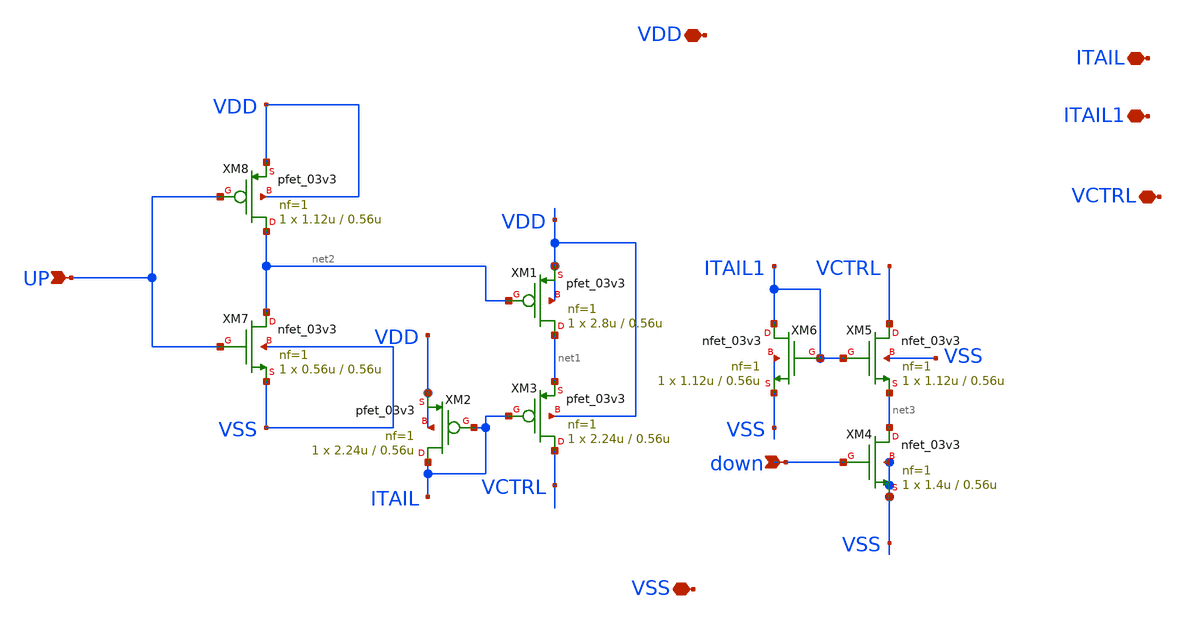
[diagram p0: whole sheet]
** sch_path: PLL-main/schematic/xschem/CP.sch
**.subckt CP UP down VCTRL VDD VSS ITAIL1 ITAIL
*.ipin UP
*.ipin down
*.iopin VCTRL
*.iopin VDD
*.iopin VSS
*.iopin ITAIL1
*.iopin ITAIL
XM1 net1 net2 VDD VDD pfet_03v3 L=0.56u W=2.8u nf=1 ad='int((nf+1)/2) * W/nf * 0.18u' as='int((nf+2)/2) * W/nf * 0.18u'
+ pd='2*int((nf+1)/2) * (W/nf + 0.18u)' ps='2*int((nf+2)/2) * (W/nf + 0.18u)' nrd='0.18u / W' nrs='0.18u / W'
+ sa=0 sb=0 sd=0 m=1
XM3 VCTRL ITAIL net1 VDD pfet_03v3 L=0.56u W=2.24u nf=1 ad='int((nf+1)/2) * W/nf * 0.18u' as='int((nf+2)/2) * W/nf * 0.18u'
+ pd='2*int((nf+1)/2) * (W/nf + 0.18u)' ps='2*int((nf+2)/2) * (W/nf + 0.18u)' nrd='0.18u / W' nrs='0.18u / W'
+ sa=0 sb=0 sd=0 m=1
XM2 ITAIL ITAIL VDD VDD pfet_03v3 L=0.56u W=2.24u nf=1 ad='int((nf+1)/2) * W/nf * 0.18u' as='int((nf+2)/2) * W/nf * 0.18u'
+ pd='2*int((nf+1)/2) * (W/nf + 0.18u)' ps='2*int((nf+2)/2) * (W/nf + 0.18u)' nrd='0.18u / W' nrs='0.18u / W'
+ sa=0 sb=0 sd=0 m=1
XM6 ITAIL1 ITAIL1 VSS VSS nfet_03v3 L=0.56u W=1.12u nf=1 ad='int((nf+1)/2) * W/nf * 0.18u' as='int((nf+2)/2) * W/nf * 0.18u'
+ pd='2*int((nf+1)/2) * (W/nf + 0.18u)' ps='2*int((nf+2)/2) * (W/nf + 0.18u)' nrd='0.18u / W' nrs='0.18u / W'
+ sa=0 sb=0 sd=0 m=1
XM5 VCTRL ITAIL1 net3 VSS nfet_03v3 L=0.56u W=1.12u nf=1 ad='int((nf+1)/2) * W/nf * 0.18u' as='int((nf+2)/2) * W/nf * 0.18u'
+ pd='2*int((nf+1)/2) * (W/nf + 0.18u)' ps='2*int((nf+2)/2) * (W/nf + 0.18u)' nrd='0.18u / W' nrs='0.18u / W'
+ sa=0 sb=0 sd=0 m=1
XM4 net3 down VSS VSS nfet_03v3 L=0.56u W=1.4u nf=1 ad='int((nf+1)/2) * W/nf * 0.18u' as='int((nf+2)/2) * W/nf * 0.18u'
+ pd='2*int((nf+1)/2) * (W/nf + 0.18u)' ps='2*int((nf+2)/2) * (W/nf + 0.18u)' nrd='0.18u / W' nrs='0.18u / W'
+ sa=0 sb=0 sd=0 m=1
XM7 net2 UP VSS VSS nfet_03v3 L=0.56u W=0.56u nf=1 ad='int((nf+1)/2) * W/nf * 0.18u' as='int((nf+2)/2) * W/nf * 0.18u'
+ pd='2*int((nf+1)/2) * (W/nf + 0.18u)' ps='2*int((nf+2)/2) * (W/nf + 0.18u)' nrd='0.18u / W' nrs='0.18u / W'
+ sa=0 sb=0 sd=0 m=1
XM8 net2 UP VDD VDD pfet_03v3 L=0.56u W=1.12u nf=1 ad='int((nf+1)/2) * W/nf * 0.18u' as='int((nf+2)/2) * W/nf * 0.18u'
+ pd='2*int((nf+1)/2) * (W/nf + 0.18u)' ps='2*int((nf+2)/2) * (W/nf + 0.18u)' nrd='0.18u / W' nrs='0.18u / W'
+ sa=0 sb=0 sd=0 m=1
**.ends
.end
